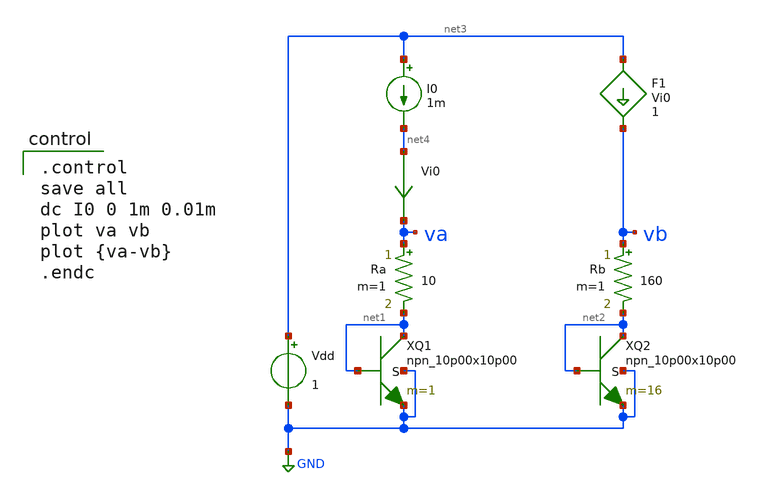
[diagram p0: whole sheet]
** sch_path: bgr/npn-diode-delta-1.sch
**.subckt npn-diode-delta-1
XQ1 net1 net1 GND GND npn_10p00x10p00 m=1
Vdd net3 GND 1
XQ2 net2 net2 GND GND npn_10p00x10p00 m=16
Rb vb net2 160 m=1
Ra va net1 10 m=1
I0 net3 net4 1m
F1 net3 vb Vi0 1
Vi0 net4 va 0
.save i(vi0)
**** begin user architecture code

.include $::180MCU_MODELS/design.ngspice
.lib $::180MCU_MODELS/sm141064.ngspice typical
.lib $::180MCU_MODELS/sm141064.ngspice res_typical
.lib $::180MCU_MODELS/sm141064.ngspice moscap_typical
.lib $::180MCU_MODELS/sm141064.ngspice bjt_typical
* .lib $::180MCU_MODELS/sm141064.ngspice res_statistical


.control
save all
dc I0 0 1m 0.01m
plot va vb
plot {va-vb}
.endc

**** end user architecture code
**.ends
.GLOBAL GND
.end
